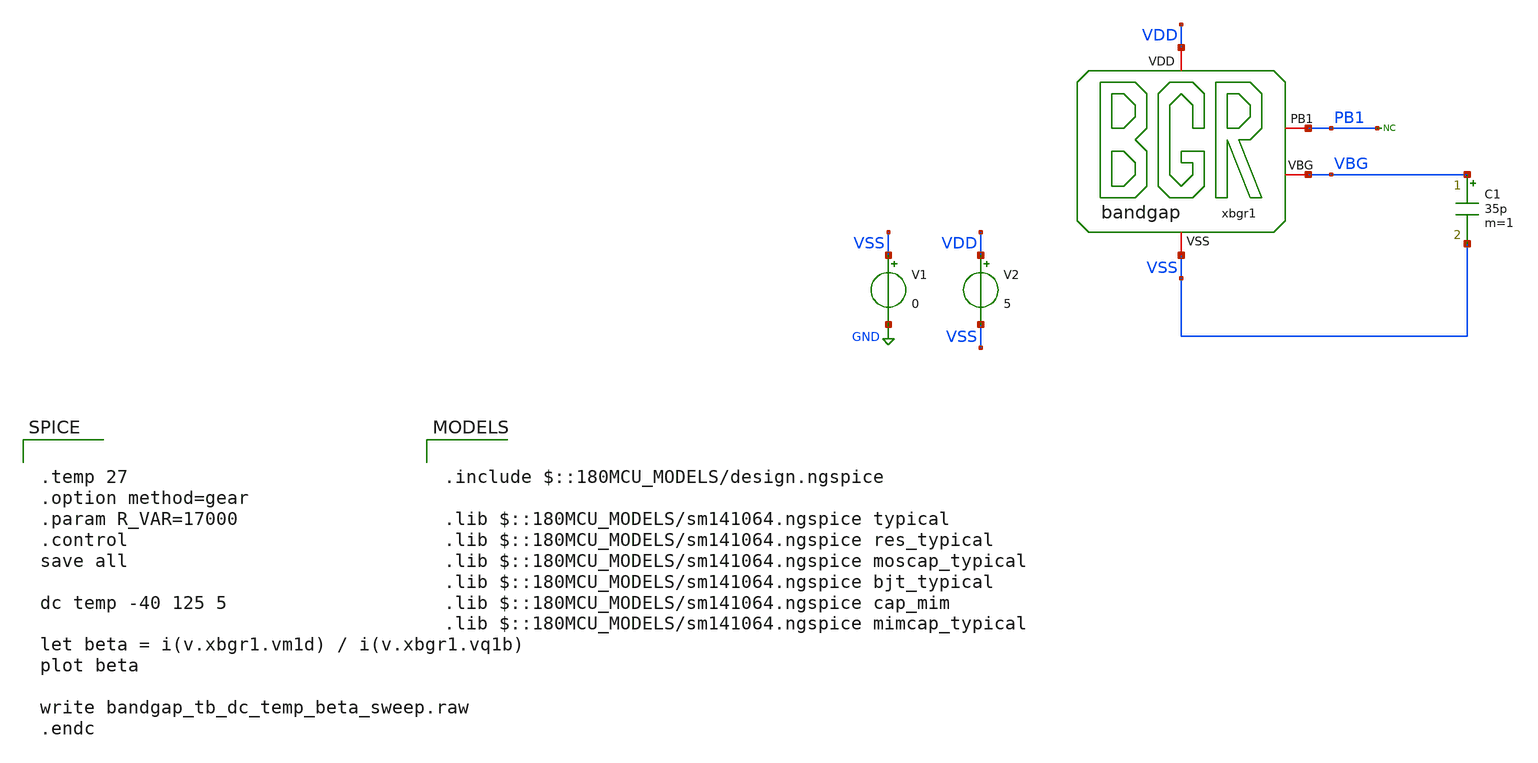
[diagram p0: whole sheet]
** sch_path: bandgap/xschem/sim/bandgap_tb_dc_temp_beta_sweep.sch
**.subckt bandgap_tb_dc_temp_beta_sweep
V1 VSS GND 0
V2 VDD VSS 5
C1 VBG VSS 35p m=1
* noconn PB1
xbgr1 VDD PB1 VBG VSS bandgap
**** begin user architecture code


.temp 27
.option method=gear
.param R_VAR=17000
.control
save all

dc temp -40 125 5

let beta = i(v.xbgr1.vm1d) / i(v.xbgr1.vq1b)
plot beta

write bandgap_tb_dc_temp_beta_sweep.raw
.endc



.include $::180MCU_MODELS/design.ngspice

.lib $::180MCU_MODELS/sm141064.ngspice typical
.lib $::180MCU_MODELS/sm141064.ngspice res_typical
.lib $::180MCU_MODELS/sm141064.ngspice moscap_typical
.lib $::180MCU_MODELS/sm141064.ngspice bjt_typical
.lib $::180MCU_MODELS/sm141064.ngspice cap_mim
.lib $::180MCU_MODELS/sm141064.ngspice mimcap_typical

**** end user architecture code
**.ends

* expanding   symbol:  bandgap/xschem/dev/bandgap.sym # of pins=4
** sym_path: bandgap/cace/testbenches/bandgap.sym
** sch_path: bandgap/cace/testbenches/bandgap.sch
.subckt bandgap VDD PB1 VBG VSS
*.iopin VSS
*.iopin VDD
*.iopin PB1
*.iopin VBG
R0 net7 VSET 1.7k m=1
R1 VSET VSS 7.6k m=1
R2 VB0 VBG 17000 m=1
XQ1 PB1 net8 net6 VSS npn_10p00x10p00 m=12
XQ0 VB0 VB0 net3 VSS npn_10p00x10p00 m=1
XM4 VSS net2 VSS VSS nfet_03v3 L=1u W=19u nf=1 ad='int((nf+1)/2) * W/nf * 0.18u' as='int((nf+2)/2) * W/nf * 0.18u'
+ pd='2*int((nf+1)/2) * (W/nf + 0.18u)' ps='2*int((nf+2)/2) * (W/nf + 0.18u)' nrd='0.18u / W' nrs='0.18u / W'
+ sa=0 sb=0 sd=0 m=1
XM2 net2 VSS VDD VDD pfet_03v3 L=10u W=1u nf=1 ad='int((nf+1)/2) * W/nf * 0.18u' as='int((nf+2)/2) * W/nf * 0.18u'
+ pd='2*int((nf+1)/2) * (W/nf + 0.18u)' ps='2*int((nf+2)/2) * (W/nf + 0.18u)' nrd='0.18u / W' nrs='0.18u / W'
+ sa=0 sb=0 sd=0 m=1
XM3 net5 net2 VDD VDD pfet_03v3 L=2u W=2u nf=1 ad='int((nf+1)/2) * W/nf * 0.18u' as='int((nf+2)/2) * W/nf * 0.18u'
+ pd='2*int((nf+1)/2) * (W/nf + 0.18u)' ps='2*int((nf+2)/2) * (W/nf + 0.18u)' nrd='0.18u / W' nrs='0.18u / W'
+ sa=0 sb=0 sd=0 m=1
XM1 net1 net1 VDD VDD pfet_03v3 L=7.4u W=20u nf=1 ad='int((nf+1)/2) * W/nf * 0.18u' as='int((nf+2)/2) * W/nf * 0.18u'
+ pd='2*int((nf+1)/2) * (W/nf + 0.18u)' ps='2*int((nf+2)/2) * (W/nf + 0.18u)' nrd='0.18u / W' nrs='0.18u / W'
+ sa=0 sb=0 sd=0 m=1
XM0 net4 net1 VDD VDD pfet_03v3 L=7.4u W=20u nf=1 ad='int((nf+1)/2) * W/nf * 0.18u' as='int((nf+2)/2) * W/nf * 0.18u'
+ pd='2*int((nf+1)/2) * (W/nf + 0.18u)' ps='2*int((nf+2)/2) * (W/nf + 0.18u)' nrd='0.18u / W' nrs='0.18u / W'
+ sa=0 sb=0 sd=0 m=1
VQ0E net3 VSET 0
VM0D net4 VB0 0
VM3D net5 VB0 0
VQ1E net6 net7 0
VM1D net1 PB1 0
VQ1B VBG net8 0
.ends

.GLOBAL GND
.end
